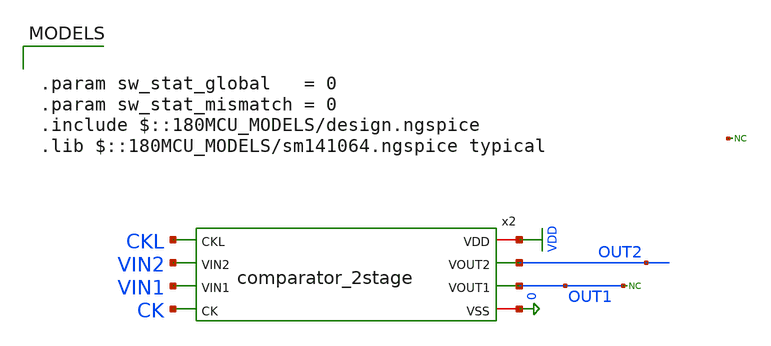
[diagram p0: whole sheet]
** sch_path: comparator_alt/schematic/strongarm_mc_tb_2.sch
**.subckt strongarm_mc_tb_2
* noconn OUT1
* noconn #net1
x2 CKL VIN2 VDD OUT2 VIN1 OUT1 CK 0 comparator_2stage
**** begin user architecture code

.param sw_stat_global   = 0
.param sw_stat_mismatch = 0
.include $::180MCU_MODELS/design.ngspice
.lib $::180MCU_MODELS/sm141064.ngspice typical




* ===== stimulus (converted from source symbols to code-block sources) =====
Vvdd  VDD  0 3.3
Vvin1 VIN1 0 PWL(0 1.2 6e-6 1.2)        ; MUST be named Vvin1 and be PWL -> alter @vvin1[pwl]
+ targets it
Vvin2 VIN2 0 1.2
Vck   CK   0 PULSE(0 3.3 2n 100p 100p 8n 20n)
Vckl  CKL  0 PULSE(0 3.3 2n 100p 100p 8n 20n)

.control
* ============================================================
* Two-stage comparator (preamp + StrongARM) — offset Monte Carlo
* ============================================================
let mc_runs = 100
let svt_pre = 0.78e-3    ; preamp input pair (64 um^2)
let svt_sa  = 3.58e-3    ; StrongARM input pair (3 um^2)
let run     = 0
let offset_results = vector(mc_runs)
let ngood = 0
let sumx  = 0
let sumx2 = 0
set homeplot = $curplot
dowhile run < mc_runs
  echo ---- run $&run ----
  unset s_up
  unset s_dn
  * fresh mismatch draw each run, on BOTH input pairs
  alter @m.x1.x1.xm1p.m0[delvto] = svt_pre * sgauss(0)
  alter @m.x1.x1.xm2p.m0[delvto] = svt_pre * sgauss(0)
  alter @m.x1.x2.xm10.m0[delvto] = svt_sa  * sgauss(0)
  alter @m.x1.x2.xm8.m0[delvto]  = svt_sa  * sgauss(0)
  * -------- UP sweep: VIN1 1.15 -> 1.25 --------
  alter @vvin1[pwl] = [ 0 1.15 6e-6 1.25 ]
  tran 10p 6u
  let t_up = -1
  meas tran t_up when v(out2)=1.5 fall=LAST
  if t_up > 0
    meas tran vin_up find v(vin1) at=t_up
    set s_up = $&vin_up
  end
  destroy $curplot
  * -------- DOWN sweep: VIN1 1.25 -> 1.15 --------
  alter @vvin1[pwl] = [ 0 1.25 6e-6 1.15 ]
  tran 10p 6u
  let t_dn = -1
  meas tran t_dn when v(out2)=1.5 fall=1
  if t_dn > 0
    meas tran vin_dn find v(vin1) at=t_dn
    set s_dn = $&vin_dn
  end
  destroy $curplot
  * -------- combine, back in the home plot --------
  setplot $homeplot
  if $?s_up * $?s_dn
    let cur = (($s_up - 1.2) + ($s_dn - 1.2)) / 2
    let offset_results[run] = cur
    let ngood = ngood + 1
    let sumx  = sumx  + cur
    let sumx2 = sumx2 + cur*cur
    echo   up=$s_up dn=$s_dn offset=$&cur
  else
    let offset_results[run] = -999
    echo   WARN: miss on run $&run
  end
  let run = run + 1
end
setplot $homeplot
let mu  = sumx / ngood
let sig = sqrt( sumx2/ngood - mu*mu )
echo ======================================================
echo MC done: N=$&mc_runs  good=$&ngood
echo   mean offset = $&mu V
echo   sigma       = $&sig V
echo ======================================================
unset wr_singlescale
write  /foss/designs/comparator/comp2_mc_offsets.raw offset_results
wrdata /foss/designs/comparator/comp2_mc_offsets.txt offset_results
echo MC N=$&mc_runs good=$&ngood mean=$&mu sigma=$&sig >
+ /foss/designs/comparator/comp2_mc_report.txt
print offset_results >> /foss/designs/comparator/comp2_mc_report.txt
.endc


**** end user architecture code
**.ends

* expanding   symbol:  comparator_2stage.sym # of pins=8
** sym_path: comparator/schematic/comparator_2stage.sym
** sch_path: comparator/schematic/comparator_2stage.sch
.subckt comparator_2stage CKL VIN2 VDD VOUT2 VIN1 VOUT1 CK VSS
*.ipin CK
*.iopin VDD
*.iopin VSS
*.ipin VIN1
*.ipin VIN2
*.opin VOUT2
*.opin VOUT1
*.ipin CKL
x2 VDD DIP1 DIP2 VIN2 VIN1 CK VSS preamp_dyn
x4 VDD CKL VOUT2 VOUT1 DIP2 DIP1 VSS strongarm_2
.ends


* expanding   symbol:  comparator/schematic/preamp_dyn.sym # of pins=7
** sym_path: comparator_alt/schematic/preamp_dyn.sym
** sch_path: comparator_alt/schematic/preamp_dyn.sch
.subckt preamp_dyn VDD DIP2 DIP1 VIN2 VIN1 CK VSS
*.ipin VIN1
*.ipin VIN2
*.iopin VDD
*.iopin VSS
*.opin DIP1
*.opin DIP2
*.ipin CK
XM1P DIP1 VIN1 TAIL VSS nfet_03v3 L=1u W=4u nf=1 ad='int((nf+1)/2) * W/nf * 0.18u' as='int((nf+2)/2) * W/nf * 0.18u'
+ pd='2*int((nf+1)/2) * (W/nf + 0.18u)' ps='2*int((nf+2)/2) * (W/nf + 0.18u)' nrd='0.18u / W' nrs='0.18u / W'
+ sa=0 sb=0 sd=0 m=16
XMT1 TAIL CK VSS VSS nfet_03v3 L=1u W=1u nf=1 ad='int((nf+1)/2) * W/nf * 0.18u' as='int((nf+2)/2) * W/nf * 0.18u'
+ pd='2*int((nf+1)/2) * (W/nf + 0.18u)' ps='2*int((nf+2)/2) * (W/nf + 0.18u)' nrd='0.18u / W' nrs='0.18u / W'
+ sa=0 sb=0 sd=0 m=1
XM2P DIP2 VIN2 TAIL VSS nfet_03v3 L=1u W=4u nf=1 ad='int((nf+1)/2) * W/nf * 0.18u' as='int((nf+2)/2) * W/nf * 0.18u'
+ pd='2*int((nf+1)/2) * (W/nf + 0.18u)' ps='2*int((nf+2)/2) * (W/nf + 0.18u)' nrd='0.18u / W' nrs='0.18u / W'
+ sa=0 sb=0 sd=0 m=16
XMP1 DIP1 CK VDD VDD pfet_03v3 L=0.3u W=3u nf=1 ad='int((nf+1)/2) * W/nf * 0.18u' as='int((nf+2)/2) * W/nf * 0.18u'
+ pd='2*int((nf+1)/2) * (W/nf + 0.18u)' ps='2*int((nf+2)/2) * (W/nf + 0.18u)' nrd='0.18u / W' nrs='0.18u / W'
+ sa=0 sb=0 sd=0 m=1
XMP2 DIP2 CK VDD VDD pfet_03v3 L=0.3u W=3u nf=1 ad='int((nf+1)/2) * W/nf * 0.18u' as='int((nf+2)/2) * W/nf * 0.18u'
+ pd='2*int((nf+1)/2) * (W/nf + 0.18u)' ps='2*int((nf+2)/2) * (W/nf + 0.18u)' nrd='0.18u / W' nrs='0.18u / W'
+ sa=0 sb=0 sd=0 m=1
.ends


* expanding   symbol:  comparator/schematic/strongarm_2.sym # of pins=7
** sym_path: comparator_alt/schematic/strongarm_2.sym
** sch_path: comparator_alt/schematic/strongarm_2.sch
.subckt strongarm_2 VDD CK VOUT2 VOUT1 VIN1 VIN2 VSS
*.opin VOUT1
*.opin VOUT2
*.ipin VIN1
*.ipin VIN2
*.ipin CK
*.iopin VDD
*.iopin VSS
XM1 VOUT2 VOUT1 net1 VSS nfet_03v3 L=0.28u W=2u nf=1 ad='int((nf+1)/2) * W/nf * 0.18u' as='int((nf+2)/2) * W/nf * 0.18u'
+ pd='2*int((nf+1)/2) * (W/nf + 0.18u)' ps='2*int((nf+2)/2) * (W/nf + 0.18u)' nrd='0.18u / W' nrs='0.18u / W'
+ sa=0 sb=0 sd=0 m=1
XM2 VOUT1 VOUT2 VDD VDD pfet_03v3 L=0.28u W=0.42u nf=1 ad='int((nf+1)/2) * W/nf * 0.18u' as='int((nf+2)/2) * W/nf * 0.18u'
+ pd='2*int((nf+1)/2) * (W/nf + 0.18u)' ps='2*int((nf+2)/2) * (W/nf + 0.18u)' nrd='0.18u / W' nrs='0.18u / W'
+ sa=0 sb=0 sd=0 m=1
XM3 VOUT1 CK VDD VDD pfet_03v3 L=0.28u W=5u nf=1 ad='int((nf+1)/2) * W/nf * 0.18u' as='int((nf+2)/2) * W/nf * 0.18u'
+ pd='2*int((nf+1)/2) * (W/nf + 0.18u)' ps='2*int((nf+2)/2) * (W/nf + 0.18u)' nrd='0.18u / W' nrs='0.18u / W'
+ sa=0 sb=0 sd=0 m=1
XM4 net3 CK VDD VDD pfet_03v3 L=0.28u W=5u nf=1 ad='int((nf+1)/2) * W/nf * 0.18u' as='int((nf+2)/2) * W/nf * 0.18u'
+ pd='2*int((nf+1)/2) * (W/nf + 0.18u)' ps='2*int((nf+2)/2) * (W/nf + 0.18u)' nrd='0.18u / W' nrs='0.18u / W'
+ sa=0 sb=0 sd=0 m=1
XM5 net1 CK VDD VDD pfet_03v3 L=0.28u W=5u nf=1 ad='int((nf+1)/2) * W/nf * 0.18u' as='int((nf+2)/2) * W/nf * 0.18u'
+ pd='2*int((nf+1)/2) * (W/nf + 0.18u)' ps='2*int((nf+2)/2) * (W/nf + 0.18u)' nrd='0.18u / W' nrs='0.18u / W'
+ sa=0 sb=0 sd=0 m=1
XM6 VOUT2 CK VDD VDD pfet_03v3 L=0.28u W=5u nf=1 ad='int((nf+1)/2) * W/nf * 0.18u' as='int((nf+2)/2) * W/nf * 0.18u'
+ pd='2*int((nf+1)/2) * (W/nf + 0.18u)' ps='2*int((nf+2)/2) * (W/nf + 0.18u)' nrd='0.18u / W' nrs='0.18u / W'
+ sa=0 sb=0 sd=0 m=1
XM7 VOUT2 VOUT1 VDD VDD pfet_03v3 L=0.28u W=0.42u nf=1 ad='int((nf+1)/2) * W/nf * 0.18u' as='int((nf+2)/2) * W/nf * 0.18u'
+ pd='2*int((nf+1)/2) * (W/nf + 0.18u)' ps='2*int((nf+2)/2) * (W/nf + 0.18u)' nrd='0.18u / W' nrs='0.18u / W'
+ sa=0 sb=0 sd=0 m=1
XM8 net1 VIN2 net2 VSS nfet_03v3 L=1u W=8u nf=1 ad='int((nf+1)/2) * W/nf * 0.18u' as='int((nf+2)/2) * W/nf * 0.18u'
+ pd='2*int((nf+1)/2) * (W/nf + 0.18u)' ps='2*int((nf+2)/2) * (W/nf + 0.18u)' nrd='0.18u / W' nrs='0.18u / W'
+ sa=0 sb=0 sd=0 m=1
XM9 VOUT1 VOUT2 net3 VSS nfet_03v3 L=0.28u W=2u nf=1 ad='int((nf+1)/2) * W/nf * 0.18u' as='int((nf+2)/2) * W/nf * 0.18u'
+ pd='2*int((nf+1)/2) * (W/nf + 0.18u)' ps='2*int((nf+2)/2) * (W/nf + 0.18u)' nrd='0.18u / W' nrs='0.18u / W'
+ sa=0 sb=0 sd=0 m=1
XM10 net3 VIN1 net2 VSS nfet_03v3 L=1u W=8u nf=1 ad='int((nf+1)/2) * W/nf * 0.18u' as='int((nf+2)/2) * W/nf * 0.18u'
+ pd='2*int((nf+1)/2) * (W/nf + 0.18u)' ps='2*int((nf+2)/2) * (W/nf + 0.18u)' nrd='0.18u / W' nrs='0.18u / W'
+ sa=0 sb=0 sd=0 m=1
XM11 net2 CK VSS VSS nfet_03v3 L=0.28u W=2u nf=1 ad='int((nf+1)/2) * W/nf * 0.18u' as='int((nf+2)/2) * W/nf * 0.18u'
+ pd='2*int((nf+1)/2) * (W/nf + 0.18u)' ps='2*int((nf+2)/2) * (W/nf + 0.18u)' nrd='0.18u / W' nrs='0.18u / W'
+ sa=0 sb=0 sd=0 m=1
.ends

.GLOBAL VDD
.end
